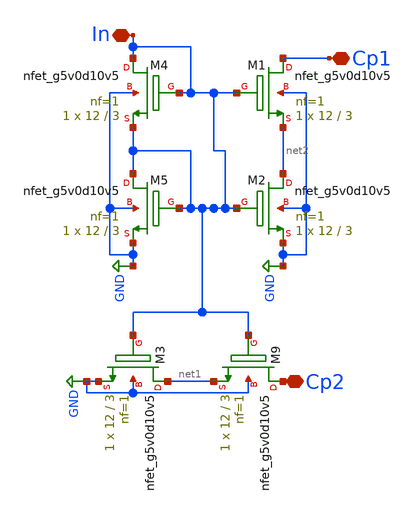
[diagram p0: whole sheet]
** sch_path: xschem/untitled-4.sch
**.subckt untitled-4 In Cp1 Cp2
*.iopin In
*.iopin Cp1
*.iopin Cp2
XM1 Cp1 In net2 GND sky130_fd_pr__nfet_g5v0d10v5 L=3 W=12 nf=1 ad='int((nf+1)/2) * W/nf * 0.29' as='int((nf+2)/2) * W/nf * 0.29'
+ pd='2*int((nf+1)/2) * (W/nf + 0.29)' ps='2*int((nf+2)/2) * (W/nf + 0.29)' nrd='0.29 / W' nrs='0.29 / W'
+ sa=0 sb=0 sd=0 mult=1 m=1
XM2 net2 In GND GND sky130_fd_pr__nfet_g5v0d10v5 L=3 W=12 nf=1 ad='int((nf+1)/2) * W/nf * 0.29' as='int((nf+2)/2) * W/nf * 0.29'
+ pd='2*int((nf+1)/2) * (W/nf + 0.29)' ps='2*int((nf+2)/2) * (W/nf + 0.29)' nrd='0.29 / W' nrs='0.29 / W'
+ sa=0 sb=0 sd=0 mult=1 m=1
XM9 Cp2 In net1 GND sky130_fd_pr__nfet_g5v0d10v5 L=3 W=12 nf=1 ad='int((nf+1)/2) * W/nf * 0.29' as='int((nf+2)/2) * W/nf * 0.29'
+ pd='2*int((nf+1)/2) * (W/nf + 0.29)' ps='2*int((nf+2)/2) * (W/nf + 0.29)' nrd='0.29 / W' nrs='0.29 / W'
+ sa=0 sb=0 sd=0 mult=1 m=1
XM3 net1 In GND GND sky130_fd_pr__nfet_g5v0d10v5 L=3 W=12 nf=1 ad='int((nf+1)/2) * W/nf * 0.29' as='int((nf+2)/2) * W/nf * 0.29'
+ pd='2*int((nf+1)/2) * (W/nf + 0.29)' ps='2*int((nf+2)/2) * (W/nf + 0.29)' nrd='0.29 / W' nrs='0.29 / W'
+ sa=0 sb=0 sd=0 mult=1 m=1
XM4 In In In GND sky130_fd_pr__nfet_g5v0d10v5 L=3 W=12 nf=1 ad='int((nf+1)/2) * W/nf * 0.29' as='int((nf+2)/2) * W/nf * 0.29'
+ pd='2*int((nf+1)/2) * (W/nf + 0.29)' ps='2*int((nf+2)/2) * (W/nf + 0.29)' nrd='0.29 / W' nrs='0.29 / W'
+ sa=0 sb=0 sd=0 mult=1 m=1
XM5 In In GND GND sky130_fd_pr__nfet_g5v0d10v5 L=3 W=12 nf=1 ad='int((nf+1)/2) * W/nf * 0.29' as='int((nf+2)/2) * W/nf * 0.29'
+ pd='2*int((nf+1)/2) * (W/nf + 0.29)' ps='2*int((nf+2)/2) * (W/nf + 0.29)' nrd='0.29 / W' nrs='0.29 / W'
+ sa=0 sb=0 sd=0 mult=1 m=1
**.ends
.GLOBAL GND
.end
